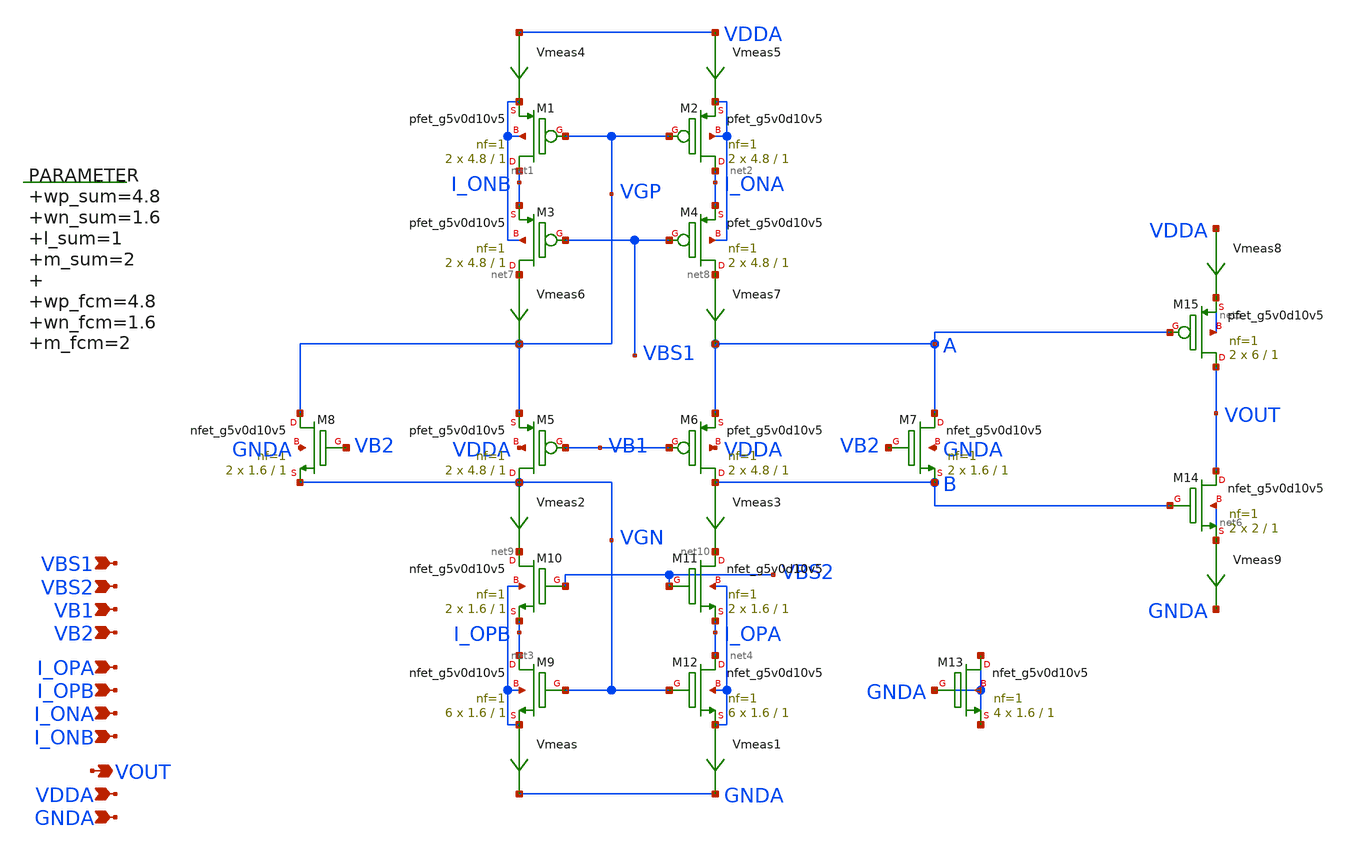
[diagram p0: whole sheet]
** sch_path: xschem/folded_cascode.sch
**.subckt folded_cascode I_OPA I_OPB I_ONA I_ONB VOUT VBS1 VBS2 VB1 VB2 VDDA GNDA
*.ipin I_OPA
*.ipin I_OPB
*.ipin I_ONA
*.ipin I_ONB
*.opin VOUT
*.ipin VBS1
*.ipin VBS2
*.ipin VB1
*.ipin VB2
*.ipin VDDA
*.ipin GNDA
.param wp_sum=4.8 wn_sum=1.6 l_sum=1 m_sum=2 wp_fcm=4.8 wn_fcm=1.6 m_fcm=2

XM1 I_ONB VGP net1 net1 sky130_fd_pr__pfet_g5v0d10v5 L=1 W=4.8 nf=1 ad='int((nf+1)/2) * W/nf * 0.29'
+ as='int((nf+2)/2) * W/nf * 0.29' pd='2*int((nf+1)/2) * (W/nf + 0.29)' ps='2*int((nf+2)/2) * (W/nf + 0.29)'
+ nrd='0.29 / W' nrs='0.29 / W' sa=0 sb=0 sd=0 mult=2 m=2
XM8 VGP VB2 VGN GNDA sky130_fd_pr__nfet_g5v0d10v5 L=1 W=1.6 nf=1 ad='int((nf+1)/2) * W/nf * 0.29' as='int((nf+2)/2) * W/nf * 0.29'
+ pd='2*int((nf+1)/2) * (W/nf + 0.29)' ps='2*int((nf+2)/2) * (W/nf + 0.29)' nrd='0.29 / W' nrs='0.29 / W'
+ sa=0 sb=0 sd=0 mult=2 m=2
XM13 GNDA GNDA GNDA GNDA sky130_fd_pr__nfet_g5v0d10v5 L=1 W=1.6 nf=1 ad='int((nf+1)/2) * W/nf * 0.29'
+ as='int((nf+2)/2) * W/nf * 0.29' pd='2*int((nf+1)/2) * (W/nf + 0.29)' ps='2*int((nf+2)/2) * (W/nf + 0.29)'
+ nrd='0.29 / W' nrs='0.29 / W' sa=0 sb=0 sd=0 mult=4 m=4
XM2 I_ONA VGP net2 net2 sky130_fd_pr__pfet_g5v0d10v5 L=1 W=4.8 nf=1 ad='int((nf+1)/2) * W/nf * 0.29'
+ as='int((nf+2)/2) * W/nf * 0.29' pd='2*int((nf+1)/2) * (W/nf + 0.29)' ps='2*int((nf+2)/2) * (W/nf + 0.29)'
+ nrd='0.29 / W' nrs='0.29 / W' sa=0 sb=0 sd=0 mult=2 m=2
XM3 net7 VBS1 I_ONB net1 sky130_fd_pr__pfet_g5v0d10v5 L=1 W=4.8 nf=1 ad='int((nf+1)/2) * W/nf * 0.29'
+ as='int((nf+2)/2) * W/nf * 0.29' pd='2*int((nf+1)/2) * (W/nf + 0.29)' ps='2*int((nf+2)/2) * (W/nf + 0.29)'
+ nrd='0.29 / W' nrs='0.29 / W' sa=0 sb=0 sd=0 mult=2 m=2
XM4 net8 VBS1 I_ONA net2 sky130_fd_pr__pfet_g5v0d10v5 L=1 W=4.8 nf=1 ad='int((nf+1)/2) * W/nf * 0.29'
+ as='int((nf+2)/2) * W/nf * 0.29' pd='2*int((nf+1)/2) * (W/nf + 0.29)' ps='2*int((nf+2)/2) * (W/nf + 0.29)'
+ nrd='0.29 / W' nrs='0.29 / W' sa=0 sb=0 sd=0 mult=2 m=2
XM5 VGN VB1 VGP VDDA sky130_fd_pr__pfet_g5v0d10v5 L=1 W=4.8 nf=1 ad='int((nf+1)/2) * W/nf * 0.29' as='int((nf+2)/2) * W/nf * 0.29'
+ pd='2*int((nf+1)/2) * (W/nf + 0.29)' ps='2*int((nf+2)/2) * (W/nf + 0.29)' nrd='0.29 / W' nrs='0.29 / W'
+ sa=0 sb=0 sd=0 mult=2 m=2
XM6 B VB1 A VDDA sky130_fd_pr__pfet_g5v0d10v5 L=1 W=4.8 nf=1 ad='int((nf+1)/2) * W/nf * 0.29' as='int((nf+2)/2) * W/nf * 0.29'
+ pd='2*int((nf+1)/2) * (W/nf + 0.29)' ps='2*int((nf+2)/2) * (W/nf + 0.29)' nrd='0.29 / W' nrs='0.29 / W'
+ sa=0 sb=0 sd=0 mult=2 m=2
XM7 A VB2 B GNDA sky130_fd_pr__nfet_g5v0d10v5 L=1 W=1.6 nf=1 ad='int((nf+1)/2) * W/nf * 0.29' as='int((nf+2)/2) * W/nf * 0.29'
+ pd='2*int((nf+1)/2) * (W/nf + 0.29)' ps='2*int((nf+2)/2) * (W/nf + 0.29)' nrd='0.29 / W' nrs='0.29 / W'
+ sa=0 sb=0 sd=0 mult=2 m=2
XM10 net9 VBS2 I_OPB net3 sky130_fd_pr__nfet_g5v0d10v5 L=1 W=1.6 nf=1 ad='int((nf+1)/2) * W/nf * 0.29'
+ as='int((nf+2)/2) * W/nf * 0.29' pd='2*int((nf+1)/2) * (W/nf + 0.29)' ps='2*int((nf+2)/2) * (W/nf + 0.29)'
+ nrd='0.29 / W' nrs='0.29 / W' sa=0 sb=0 sd=0 mult=2 m=2
XM11 net10 VBS2 I_OPA net4 sky130_fd_pr__nfet_g5v0d10v5 L=1 W=1.6 nf=1 ad='int((nf+1)/2) * W/nf * 0.29'
+ as='int((nf+2)/2) * W/nf * 0.29' pd='2*int((nf+1)/2) * (W/nf + 0.29)' ps='2*int((nf+2)/2) * (W/nf + 0.29)'
+ nrd='0.29 / W' nrs='0.29 / W' sa=0 sb=0 sd=0 mult=2 m=2
XM9 I_OPB VGN net3 net3 sky130_fd_pr__nfet_g5v0d10v5 L=1 W=1.6 nf=1 ad='int((nf+1)/2) * W/nf * 0.29'
+ as='int((nf+2)/2) * W/nf * 0.29' pd='2*int((nf+1)/2) * (W/nf + 0.29)' ps='2*int((nf+2)/2) * (W/nf + 0.29)'
+ nrd='0.29 / W' nrs='0.29 / W' sa=0 sb=0 sd=0 mult=6 m=6
XM12 I_OPA VGN net4 net4 sky130_fd_pr__nfet_g5v0d10v5 L=1 W=1.6 nf=1 ad='int((nf+1)/2) * W/nf * 0.29'
+ as='int((nf+2)/2) * W/nf * 0.29' pd='2*int((nf+1)/2) * (W/nf + 0.29)' ps='2*int((nf+2)/2) * (W/nf + 0.29)'
+ nrd='0.29 / W' nrs='0.29 / W' sa=0 sb=0 sd=0 mult=6 m=6
XM14 VOUT B net6 net6 sky130_fd_pr__nfet_g5v0d10v5 L=1 W=2 nf=1 ad='int((nf+1)/2) * W/nf * 0.29' as='int((nf+2)/2) * W/nf * 0.29'
+ pd='2*int((nf+1)/2) * (W/nf + 0.29)' ps='2*int((nf+2)/2) * (W/nf + 0.29)' nrd='0.29 / W' nrs='0.29 / W'
+ sa=0 sb=0 sd=0 mult=2 m=2
XM15 VOUT A net5 net5 sky130_fd_pr__pfet_g5v0d10v5 L=1 W=6 nf=1 ad='int((nf+1)/2) * W/nf * 0.29' as='int((nf+2)/2) * W/nf * 0.29'
+ pd='2*int((nf+1)/2) * (W/nf + 0.29)' ps='2*int((nf+2)/2) * (W/nf + 0.29)' nrd='0.29 / W' nrs='0.29 / W'
+ sa=0 sb=0 sd=0 mult=2 m=2
Vmeas net3 GNDA 0
.save i(vmeas)
Vmeas1 net4 GNDA 0
.save i(vmeas1)
Vmeas2 VGN net9 0
.save i(vmeas2)
Vmeas3 B net10 0
.save i(vmeas3)
Vmeas4 VDDA net1 0
.save i(vmeas4)
Vmeas5 VDDA net2 0
.save i(vmeas5)
Vmeas6 net7 VGP 0
.save i(vmeas6)
Vmeas7 net8 A 0
.save i(vmeas7)
Vmeas8 VDDA net5 0
.save i(vmeas8)
Vmeas9 net6 GNDA 0
.save i(vmeas9)
**.ends
.end
